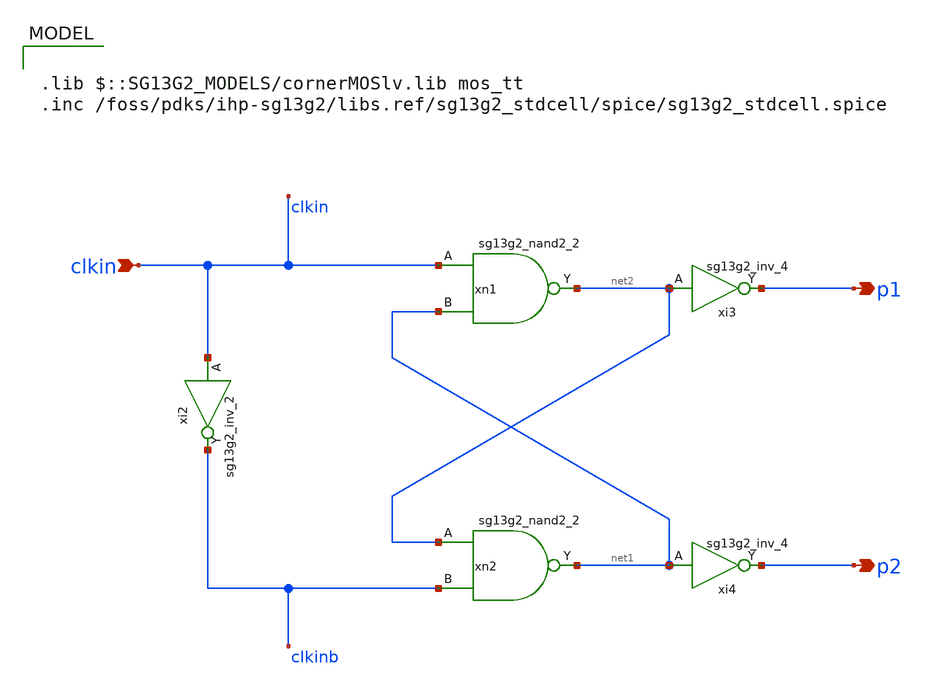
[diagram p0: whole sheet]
** sch_path: DSM_1storder/Schematic_Level/xschem/ClkG.sch
* IHP-GmbH/IHP-Open-PDK/ihp-sg13g2/libs.tech/xschem/sg13g2_stdcells/sg13g2_inv_2.sch:
* Copyright 2023 IHP PDK Authors
* Licensed under the Apache License, Version 2.0 (the "License");
**.subckt ClkG clkin p1 p2
*.ipin clkin
*.opin p1
*.opin p2
xn1 net2 clkin net1 VDD VSS sg13g2_nand2_2
xi2 clkinb clkin VDD VSS sg13g2_inv_2
xn2 net1 net2 clkinb VDD VSS sg13g2_nand2_2
xi3 p1 net2 VDD VSS sg13g2_inv_4
xi4 p2 net1 VDD VSS sg13g2_inv_4
**** begin user architecture code

.lib $::SG13G2_MODELS/cornerMOSlv.lib mos_tt
.inc /foss/pdks/ihp-sg13g2/libs.ref/sg13g2_stdcell/spice/sg13g2_stdcell.spice

**** end user architecture code
**.ends

* expanding   symbol:  sg13g2_stdcells/sg13g2_nand2_2.sym # of pins=3
** sym_path: sg13g2_stdcells/sg13g2_nand2_2.sym
** sch_path: sg13g2_stdcells/sg13g2_nand2_2.sch
.subckt sg13g2_nand2_2 Y A B VDD VSS
*.iopin VDD
*.iopin VSS
*.opin Y
*.ipin B
*.ipin A
XM1 Y A net1 VSS sg13_lv_nmos w=1.44u l=130.00n ng=2 m=1 mm_ok=1
XM2 net1 B VSS VSS sg13_lv_nmos w=1.44u l=130.00n ng=2 m=1 mm_ok=1
XM3 Y A VDD VDD sg13_lv_pmos w=2.24u l=130.00n ng=2 m=1 mm_ok=1
XM4 Y B VDD VDD sg13_lv_pmos w=2.24u l=130.00n ng=2 m=1 mm_ok=1
.ends


* expanding   symbol:  sg13g2_stdcells/sg13g2_inv_2.sym # of pins=2
** sym_path: sg13g2_stdcells/sg13g2_inv_2.sym
** sch_path: sg13g2_stdcells/sg13g2_inv_2.sch
.subckt sg13g2_inv_2 Y A VDD VSS
*.opin Y
*.ipin A
*.iopin VDD
*.iopin VSS
XM1 Y A VSS VSS sg13_lv_nmos w=1.48u l=130.00n ng=2 m=1 mm_ok=1
XM2 Y A VDD VDD sg13_lv_pmos w=2.24u l=130.00n ng=2 m=1 mm_ok=1
.ends


* expanding   symbol:  sg13g2_stdcells/sg13g2_inv_4.sym # of pins=2
** sym_path: sg13g2_stdcells/sg13g2_inv_4.sym
** sch_path: sg13g2_stdcells/sg13g2_inv_4.sch
.subckt sg13g2_inv_4 Y A VDD VSS
*.ipin A
*.opin Y
*.iopin VDD
*.iopin VSS
XM1 Y A VSS VSS sg13_lv_nmos w=2.96u l=130.00n ng=4 m=1 mm_ok=1
XM2 Y A VDD VDD sg13_lv_pmos w=4.48u l=130.00n ng=4 m=1 mm_ok=1
.ends

.end
